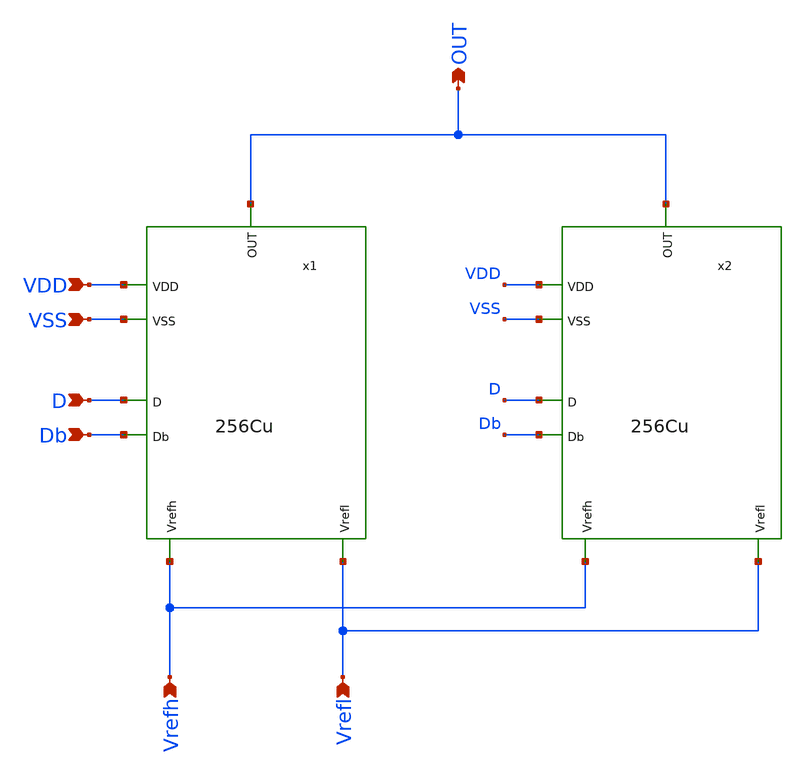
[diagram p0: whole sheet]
** sch_path: 512Cu.sch
**.subckt 512Cu OUT VDD D VSS Vrefh Vrefl Db
*.opin OUT
*.ipin VDD
*.ipin D
*.ipin VSS
*.ipin Vrefh
*.ipin Vrefl
*.ipin Db
x1 OUT VSS VDD Db D Vrefl Vrefh 256Cu
x2 OUT VSS VDD Db D Vrefl Vrefh 256Cu
**.ends
.end
